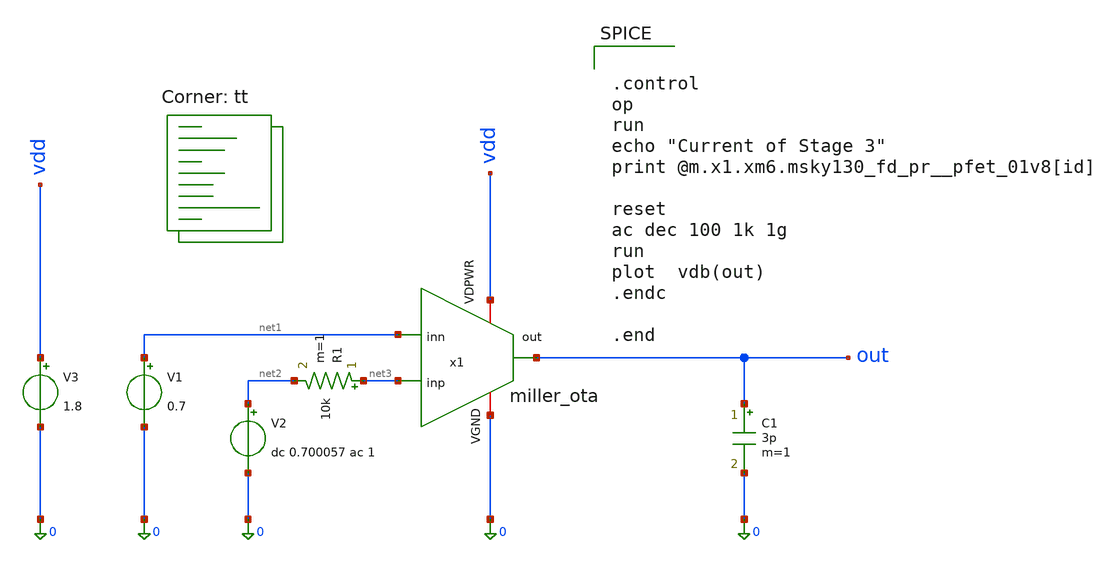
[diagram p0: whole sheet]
** sch_path: src/xschem/miller_ota_test_openLoop.sch
**.subckt miller_ota_test_openLoop
x1 vdd out net1 net3 0 miller_ota
V1 net1 0 0.7
V2 net2 0 dc 0.700057 ac 1
R1 net3 net2 10k m=1
C1 out 0 3p m=1
V3 vdd 0 1.8
**** begin user architecture code


.control
op
run
echo "Current of Stage 3"
print @m.x1.xm6.msky130_fd_pr__pfet_01v8[id]

reset
ac dec 100 1k 1g
run
plot  vdb(out)
.endc

.end

.lib $::SKYWATER_MODELS/sky130.lib.spice tt
**** end user architecture code
**.ends

* expanding   symbol:  miller_ota.sym # of pins=5
** sym_path: src/xschem/miller_ota.sym
** sch_path: src/xschem/miller_ota.sch
.subckt miller_ota VDPWR out inn inp VGND
*.ipin inp
*.opin out
*.ipin inn
*.iopin VDPWR
*.iopin VGND
XMs1 net1 net1 VDPWR VDPWR sky130_fd_pr__pfet_01v8 L=10 W=0.5 nf=1 ad='int((1 + 1)/2) * 0.5 / 1 * 0.29'
+ as='int((1 + 2)/2) * 0.5 / 1 * 0.29' pd='2*int((1 + 1)/2) * (0.5 / 1 + 0.29)' ps='2*int((1 + 2)/2) * (0.5 / 1 + 0.29)'
+ nrd='0.29 / 0.5 ' nrs='0.29 / 0.5 ' sa=0 sb=0 sd=0 mult=1 m=1
XMs3 vref net1 net2 VGND sky130_fd_pr__nfet_01v8 L=1 W=2 nf=1 ad='int((1 + 1)/2) * 2 / 1 * 0.29' as='int((1 + 2)/2) * 2 / 1 * 0.29'
+ pd='2*int((1 + 1)/2) * (2 / 1 + 0.29)' ps='2*int((1 + 2)/2) * (2 / 1 + 0.29)' nrd='0.29 / 2 ' nrs='0.29 / 2 '
+ sa=0 sb=0 sd=0 mult=1 m=1
XMs2 net1 net2 VGND VGND sky130_fd_pr__nfet_01v8 L=0.15 W=1 nf=1 ad='int((1 + 1)/2) * 1 / 1 * 0.29' as='int((1 + 2)/2) * 1 / 1 * 0.29'
+ pd='2*int((1 + 1)/2) * (1 / 1 + 0.29)' ps='2*int((1 + 2)/2) * (1 / 1 + 0.29)' nrd='0.29 / 1 ' nrs='0.29 / 1 '
+ sa=0 sb=0 sd=0 mult=1 m=1
XMr3 net2 net2 VGND VGND sky130_fd_pr__nfet_01v8 L=1 W=5 nf=1 ad='int((1 + 1)/2) * 5 / 1 * 0.29' as='int((1 + 2)/2) * 5 / 1 * 0.29'
+ pd='2*int((1 + 1)/2) * (5 / 1 + 0.29)' ps='2*int((1 + 2)/2) * (5 / 1 + 0.29)' nrd='0.29 / 5 ' nrs='0.29 / 5 '
+ sa=0 sb=0 sd=0 mult=1 m=1
XMr1 net2 vref VDPWR VDPWR sky130_fd_pr__pfet_01v8 L=1 W=10 nf=1 ad='int((1 + 1)/2) * 10 / 1 * 0.29'
+ as='int((1 + 2)/2) * 10 / 1 * 0.29' pd='2*int((1 + 1)/2) * (10 / 1 + 0.29)' ps='2*int((1 + 2)/2) * (10 / 1 + 0.29)'
+ nrd='0.29 / 10 ' nrs='0.29 / 10 ' sa=0 sb=0 sd=0 mult=1 m=1
XMr2 vref vref VDPWR VDPWR sky130_fd_pr__pfet_01v8 L=1 W=10 nf=1 ad='int((1 + 1)/2) * 10 / 1 * 0.29'
+ as='int((1 + 2)/2) * 10 / 1 * 0.29' pd='2*int((1 + 1)/2) * (10 / 1 + 0.29)' ps='2*int((1 + 2)/2) * (10 / 1 + 0.29)'
+ nrd='0.29 / 10 ' nrs='0.29 / 10 ' sa=0 sb=0 sd=0 mult=1 m=1
XMr4 vref net2 net3 net3 sky130_fd_pr__nfet_01v8 L=1 W=5 nf=1 ad='int((1 + 1)/2) * 5 / 1 * 0.29' as='int((1 + 2)/2) * 5 / 1 * 0.29'
+ pd='2*int((1 + 1)/2) * (5 / 1 + 0.29)' ps='2*int((1 + 2)/2) * (5 / 1 + 0.29)' nrd='0.29 / 5 ' nrs='0.29 / 5 '
+ sa=0 sb=0 sd=0 mult=4 m=4
XR1 VGND net3 VGND sky130_fd_pr__res_xhigh_po W=1 L=4 mult=1 m=1
XM4 net5 net4 VGND VGND sky130_fd_pr__nfet_01v8 L=2 W=0.65 nf=1 ad='int((1 + 1)/2) * 0.65 / 1 * 0.29'
+ as='int((1 + 2)/2) * 0.65 / 1 * 0.29' pd='2*int((1 + 1)/2) * (0.65 / 1 + 0.29)' ps='2*int((1 + 2)/2) * (0.65 / 1 + 0.29)'
+ nrd='0.29 / 0.65 ' nrs='0.29 / 0.65 ' sa=0 sb=0 sd=0 mult=1 m=1
XM3 net4 net4 VGND VGND sky130_fd_pr__nfet_01v8 L=2 W=0.65 nf=1 ad='int((1 + 1)/2) * 0.65 / 1 * 0.29'
+ as='int((1 + 2)/2) * 0.65 / 1 * 0.29' pd='2*int((1 + 1)/2) * (0.65 / 1 + 0.29)' ps='2*int((1 + 2)/2) * (0.65 / 1 + 0.29)'
+ nrd='0.29 / 0.65 ' nrs='0.29 / 0.65 ' sa=0 sb=0 sd=0 mult=1 m=1
XM1 net4 inn net6 net6 sky130_fd_pr__pfet_01v8_lvt L=0.5 W=1.25 nf=1 ad='int((1 + 1)/2) * 1.25 / 1 * 0.29'
+ as='int((1 + 2)/2) * 1.25 / 1 * 0.29' pd='2*int((1 + 1)/2) * (1.25 / 1 + 0.29)' ps='2*int((1 + 2)/2) * (1.25 / 1 + 0.29)'
+ nrd='0.29 / 1.25 ' nrs='0.29 / 1.25 ' sa=0 sb=0 sd=0 mult=1 m=1
XM2 net5 inp net6 net6 sky130_fd_pr__pfet_01v8_lvt L=0.5 W=1.25 nf=1 ad='int((1 + 1)/2) * 1.25 / 1 * 0.29'
+ as='int((1 + 2)/2) * 1.25 / 1 * 0.29' pd='2*int((1 + 1)/2) * (1.25 / 1 + 0.29)' ps='2*int((1 + 2)/2) * (1.25 / 1 + 0.29)'
+ nrd='0.29 / 1.25 ' nrs='0.29 / 1.25 ' sa=0 sb=0 sd=0 mult=1 m=1
XM9 net8 net8 net7 VGND sky130_fd_pr__nfet_01v8 L=2 W=0.55 nf=1 ad='int((1 + 1)/2) * 0.55 / 1 * 0.29'
+ as='int((1 + 2)/2) * 0.55 / 1 * 0.29' pd='2*int((1 + 1)/2) * (0.55 / 1 + 0.29)' ps='2*int((1 + 2)/2) * (0.55 / 1 + 0.29)'
+ nrd='0.29 / 0.55 ' nrs='0.29 / 0.55 ' sa=0 sb=0 sd=0 mult=1 m=1
XM10 net7 net7 VGND VGND sky130_fd_pr__nfet_01v8 L=2 W=0.55 nf=1 ad='int((1 + 1)/2) * 0.55 / 1 * 0.29'
+ as='int((1 + 2)/2) * 0.55 / 1 * 0.29' pd='2*int((1 + 1)/2) * (0.55 / 1 + 0.29)' ps='2*int((1 + 2)/2) * (0.55 / 1 + 0.29)'
+ nrd='0.29 / 0.55 ' nrs='0.29 / 0.55 ' sa=0 sb=0 sd=0 mult=1 m=1
XMc net9 net8 net5 VGND sky130_fd_pr__nfet_01v8 L=2 W=0.65 nf=1 ad='int((1 + 1)/2) * 0.65 / 1 * 0.29'
+ as='int((1 + 2)/2) * 0.65 / 1 * 0.29' pd='2*int((1 + 1)/2) * (0.65 / 1 + 0.29)' ps='2*int((1 + 2)/2) * (0.65 / 1 + 0.29)'
+ nrd='0.29 / 0.65 ' nrs='0.29 / 0.65 ' sa=0 sb=0 sd=0 mult=2 m=2
XC1 out net9 sky130_fd_pr__cap_mim_m3_1 W=20 L=20 MF=1 m=1
XM5 out net5 VGND VGND sky130_fd_pr__nfet_01v8 L=2 W=0.65 nf=1 ad='int((1 + 1)/2) * 0.65 / 1 * 0.29'
+ as='int((1 + 2)/2) * 0.65 / 1 * 0.29' pd='2*int((1 + 1)/2) * (0.65 / 1 + 0.29)' ps='2*int((1 + 2)/2) * (0.65 / 1 + 0.29)'
+ nrd='0.29 / 0.65 ' nrs='0.29 / 0.65 ' sa=0 sb=0 sd=0 mult=30 m=30
XM8 net8 vref VDPWR VDPWR sky130_fd_pr__pfet_01v8 L=1 W=5.6 nf=1 ad='int((1 + 1)/2) * 5.6 / 1 * 0.29'
+ as='int((1 + 2)/2) * 5.6 / 1 * 0.29' pd='2*int((1 + 1)/2) * (5.6 / 1 + 0.29)' ps='2*int((1 + 2)/2) * (5.6 / 1 + 0.29)'
+ nrd='0.29 / 5.6 ' nrs='0.29 / 5.6 ' sa=0 sb=0 sd=0 mult=2 m=2
XM7 out vref VDPWR VDPWR sky130_fd_pr__pfet_01v8 L=1 W=5.3 nf=1 ad='int((1 + 1)/2) * 5.3 / 1 * 0.29'
+ as='int((1 + 2)/2) * 5.3 / 1 * 0.29' pd='2*int((1 + 1)/2) * (5.3 / 1 + 0.29)' ps='2*int((1 + 2)/2) * (5.3 / 1 + 0.29)'
+ nrd='0.29 / 5.3 ' nrs='0.29 / 5.3 ' sa=0 sb=0 sd=0 mult=15 m=15
XM6 net6 vref VDPWR VDPWR sky130_fd_pr__pfet_01v8 L=1 W=5.3 nf=1 ad='int((1 + 1)/2) * 5.3 / 1 * 0.29'
+ as='int((1 + 2)/2) * 5.3 / 1 * 0.29' pd='2*int((1 + 1)/2) * (5.3 / 1 + 0.29)' ps='2*int((1 + 2)/2) * (5.3 / 1 + 0.29)'
+ nrd='0.29 / 5.3 ' nrs='0.29 / 5.3 ' sa=0 sb=0 sd=0 mult=1 m=1
.ends

.end
